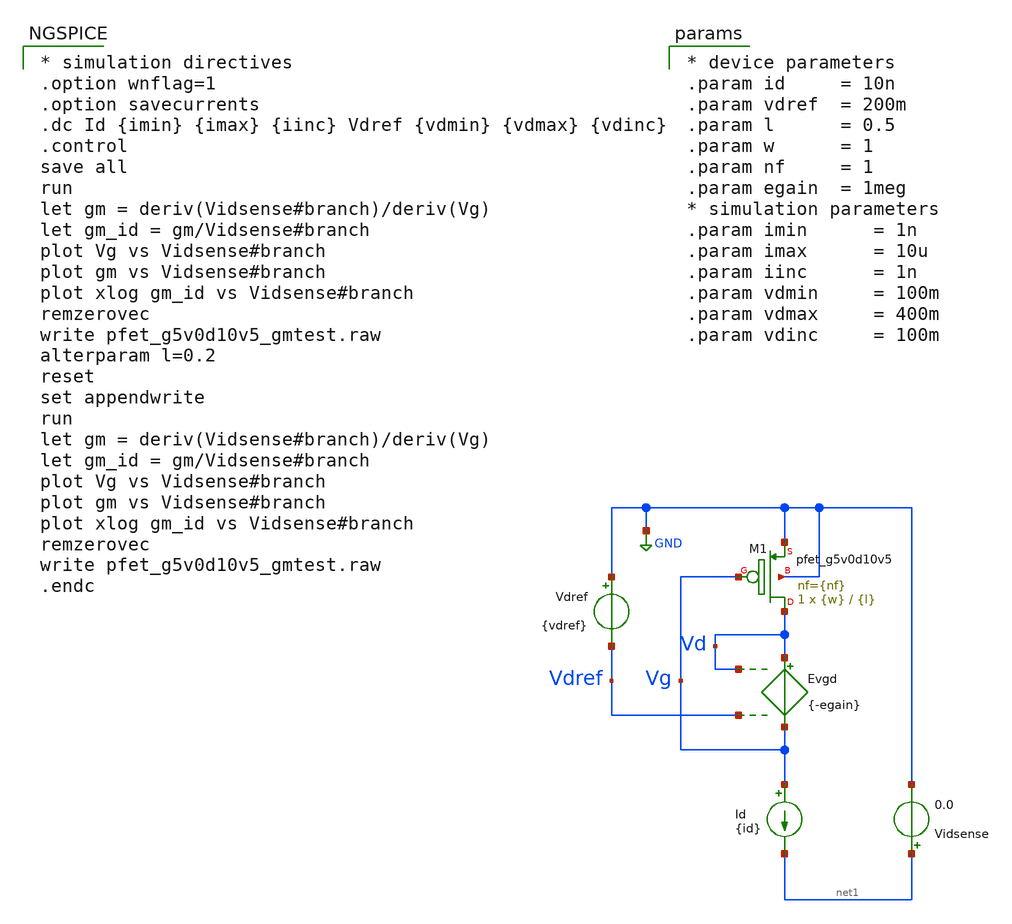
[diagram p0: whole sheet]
** sch_path: xschem/pfet_g5v0d10v5_gmtest.sch
**.subckt pfet_g5v0d10v5_gmtest
Evgd Vd Vg Vd Vdref {-egain}
Id Vg net1 {id}
Vdref GND Vdref {vdref}
Vidsense net1 GND 0.0
XM1 Vd Vg GND GND sky130_fd_pr__pfet_g5v0d10v5 L={l} W={w} nf={nf} ad='int(({nf} + 1)/2) * {w} / {nf} * 0.29'
+ as='int(({nf} + 2)/2) * {w} / {nf} * 0.29' pd='2*int(({nf} + 1)/2) * ({w} / {nf} + 0.29)' ps='2*int(({nf} + 2)/2) * ({w} / {nf} + 0.29)'
+ nrd='0.29 / {w} ' nrs='0.29 / {w} ' sa=0 sb=0 sd=0 mult=1 m=1
**** begin user architecture code

** opencircuitdesign pdks install
.lib $::SKYWATER_MODELS/sky130.lib.spice tt



* simulation directives
.option wnflag=1
.option savecurrents
.dc Id {imin} {imax} {iinc} Vdref {vdmin} {vdmax} {vdinc}
.control
save all
run
let gm = deriv(Vidsense#branch)/deriv(Vg)
let gm_id = gm/Vidsense#branch
plot Vg vs Vidsense#branch
plot gm vs Vidsense#branch
plot xlog gm_id vs Vidsense#branch
remzerovec
write pfet_g5v0d10v5_gmtest.raw
alterparam l=0.2
reset
set appendwrite
run
let gm = deriv(Vidsense#branch)/deriv(Vg)
let gm_id = gm/Vidsense#branch
plot Vg vs Vidsense#branch
plot gm vs Vidsense#branch
plot xlog gm_id vs Vidsense#branch
remzerovec
write pfet_g5v0d10v5_gmtest.raw
.endc



* device parameters
.param id     = 10n
.param vdref  = 200m
.param l      = 0.5
.param w      = 1
.param nf     = 1
.param egain  = 1meg
* simulation parameters
.param imin      = 1n
.param imax      = 10u
.param iinc      = 1n
.param vdmin     = 100m
.param vdmax     = 400m
.param vdinc     = 100m


**** end user architecture code
**.ends
.GLOBAL GND
.end
